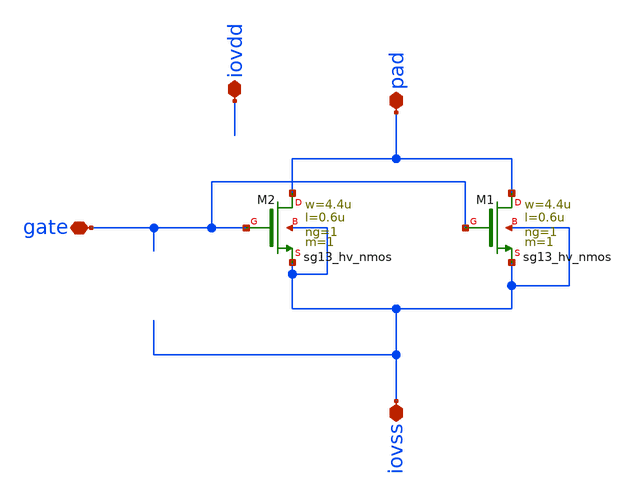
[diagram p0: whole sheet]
** sch_path: ihp-sg13g2/libs.ref/sg13g2_io/xschem/sg13g2_Clamp_N2N2D.sch
**.subckt sg13g2_Clamp_N2N2D iovss gate pad iovdd
*.iopin iovss
*.iopin gate
*.iopin pad
*.iopin iovdd
XM1 pad gate iovss iovss sg13_hv_nmos w=4.4u l=0.6u ng=1 m=1
XM2 pad gate iovss iovss sg13_hv_nmos w=4.4u l=0.6u ng=1 m=1
**.ends
.end
